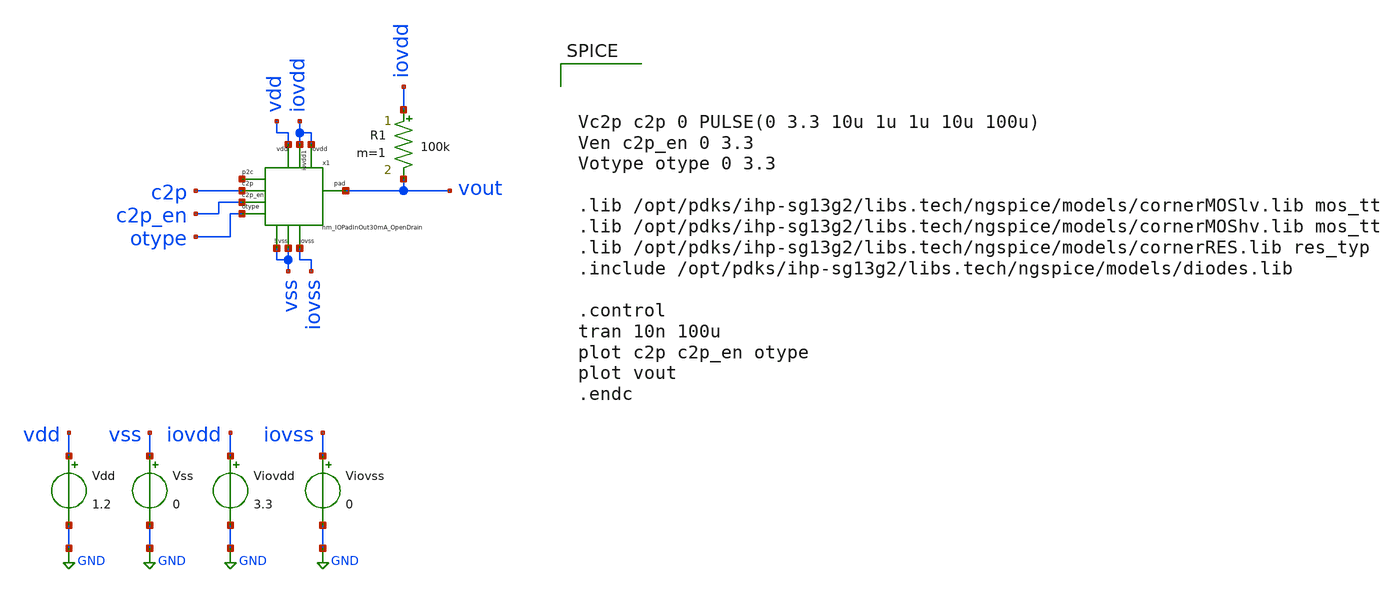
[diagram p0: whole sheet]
** sch_path: libs.tech/xschem/tests/test_hm_IOPadInOut30mA_OpenDrain.sch
**.subckt test_hm_IOPadInOut30mA_OpenDrain
x1 vss vdd vss iovss iovdd c2p vout iovdd c2p_en net1 otype hm_IOPadInOut30mA_OpenDrain
Vdd vdd GND 1.2
Vss vss GND 0
Viovdd iovdd GND 3.3
Viovss iovss GND 0
R1 iovdd vout 100k m=1
**** begin user architecture code



Vc2p c2p 0 PULSE(0 3.3 10u 1u 1u 10u 100u)
Ven c2p_en 0 3.3
Votype otype 0 3.3

.lib /opt/pdks/ihp-sg13g2/libs.tech/ngspice/models/cornerMOSlv.lib mos_tt
.lib /opt/pdks/ihp-sg13g2/libs.tech/ngspice/models/cornerMOShv.lib mos_tt
.lib /opt/pdks/ihp-sg13g2/libs.tech/ngspice/models/cornerRES.lib res_typ
.include /opt/pdks/ihp-sg13g2/libs.tech/ngspice/models/diodes.lib

.control
tran 10n 100u
plot c2p c2p_en otype
plot vout
.endc



**** end user architecture code
**.ends
.GLOBAL GND
.end
